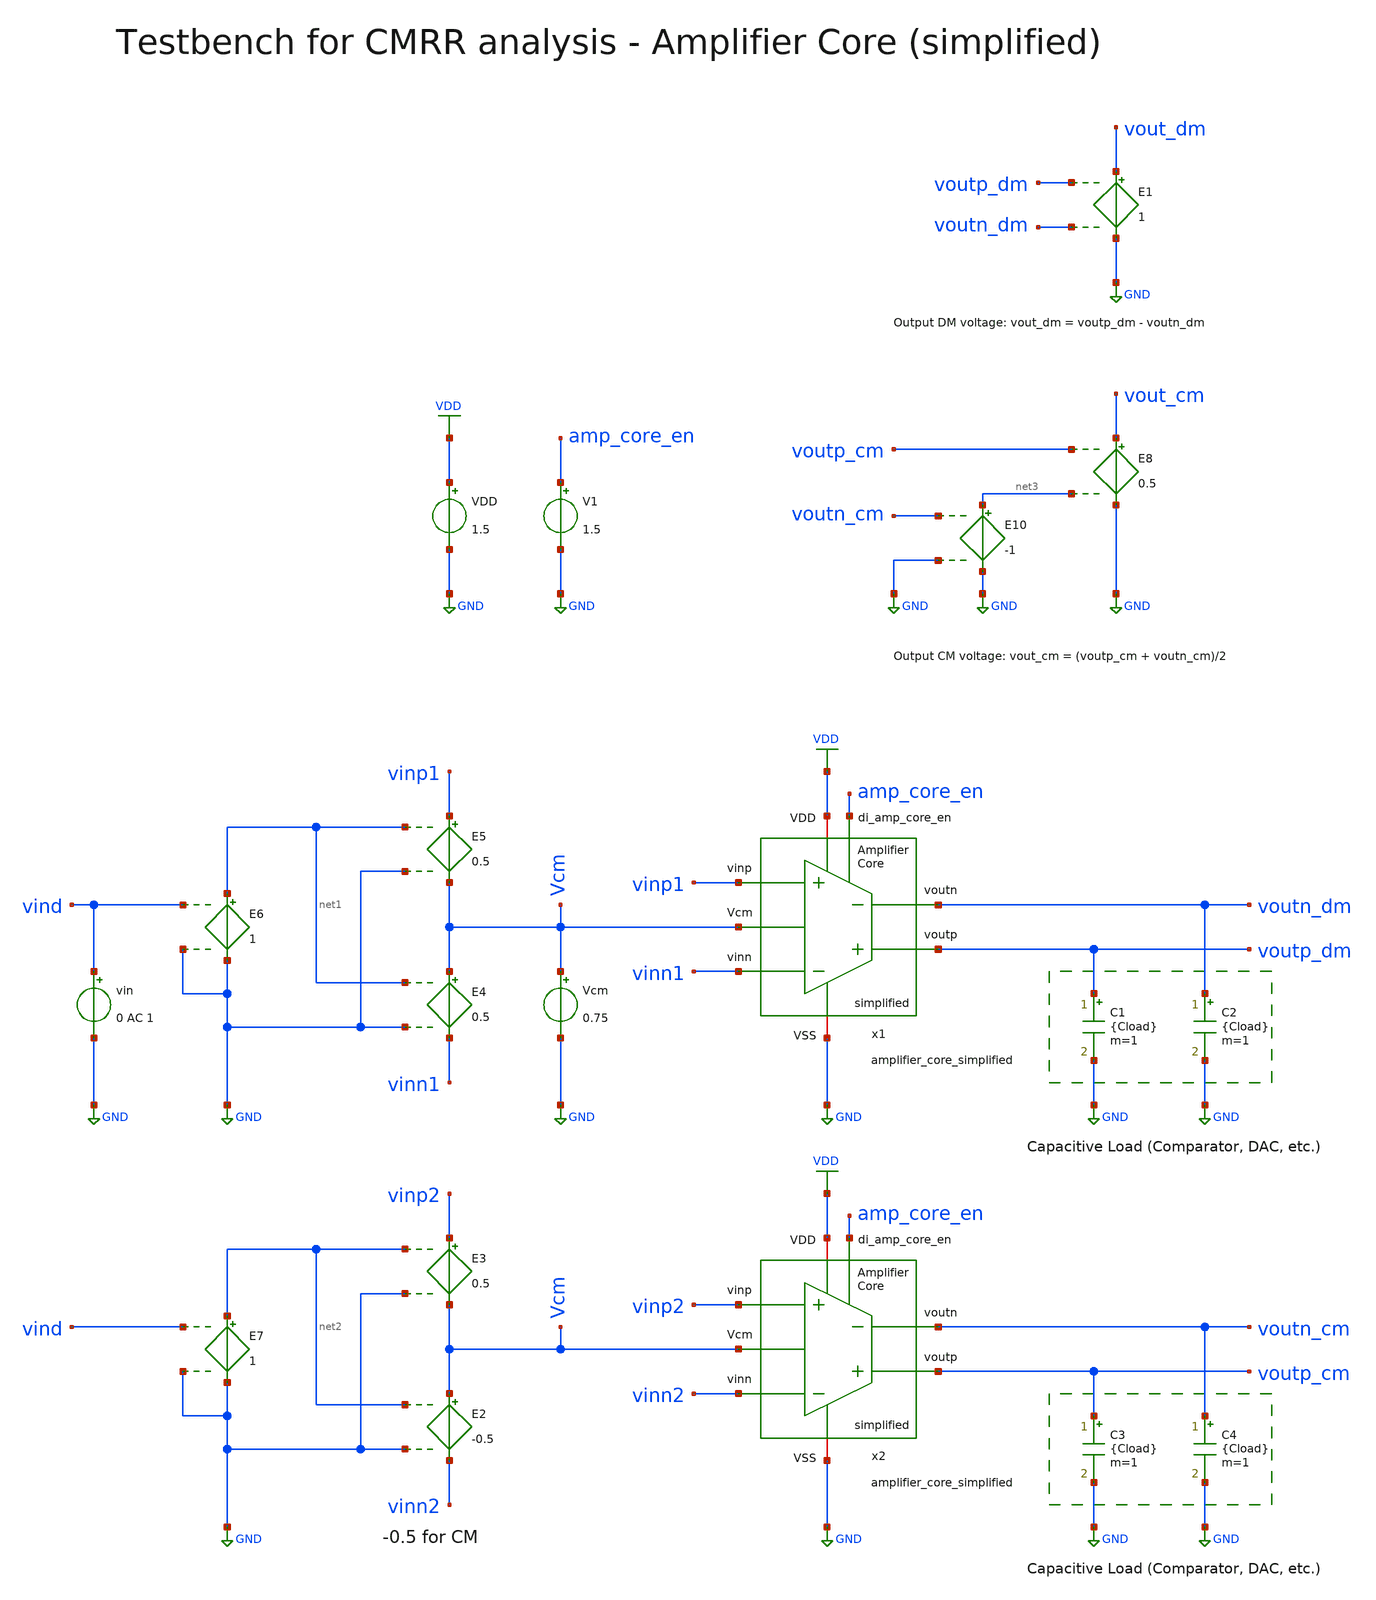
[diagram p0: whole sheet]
** sch_path: SG13G2_ATBS-ADC-main/xschem/bio_amplifier/amplifier_core/testbenches/amplifier_core_simplified_tb_CMRR.sch
**.subckt amplifier_core_simplified_tb_CMRR
VDD VDD GND 1.5
C1 voutp_dm GND {Cload} m=1
C2 voutn_dm GND {Cload} m=1
Vcm Vcm GND 0.75
E4 Vcm vinn1 net1 GND 0.5
E5 vinp1 Vcm net1 GND 0.5
E6 net1 GND vind GND 1
V1 amp_core_en GND 1.5
E1 vout_dm GND voutp_dm voutn_dm 1
vin vind GND 0 AC 1
x1 voutp_dm voutn_dm amp_core_en vinn1 vinp1 VDD GND Vcm amplifier_core_simplified
C3 voutp_cm GND {Cload} m=1
C4 voutn_cm GND {Cload} m=1
E2 Vcm vinn2 net2 GND -0.5
E3 vinp2 Vcm net2 GND 0.5
E7 net2 GND vind GND 1
x2 voutp_cm voutn_cm amp_core_en vinn2 vinp2 VDD GND Vcm amplifier_core_simplified
E8 vout_cm GND voutp_cm net3 0.5
E10 net3 GND voutn_cm GND -1
**** begin user architecture code


.param temp=27
* 228fF DAC + (1 - beta) * 3.3pF
.param Cload=3.49p
.options savecurrents method=gear reltol=1e-2 abstol=1e-15 gmin=1e-15 rshunt=1e15
.control

save v(vout_dm) v(vout_cm) v(vind)

set wr_vecnames
set wr_singlescale

* User Constants
let f_min = 10m
let f_max = 1G
let fdc = 1

* Operating Point Analysis
op
remzerovec
write amplifier_core_simplified_tb_CMRR.raw
set appendwrite

* AC Analysis
ac dec 101 $&const.f_min $&const.f_max
remzerovec
write amplifier_core_simplified_tb_CMRR.raw

* Plotting Differential Mode Gain
let Adm = v(vout_dm)/v(vind)
let Adm_dB = vdb(Adm)
let Adm_arg = 180/PI*cphase(Adm)
plot Adm_dB Adm_arg ylabel 'Magnitude, Phase'

* Plotting Common Mode Gain
let Acm = v(vout_cm)/v(vind)
let Acm_dB = vdb(Acm)
let Acm_arg = 180/PI*cphase(Acm)
plot Acm_dB Acm_arg ylabel 'Magnitude, Phase'

* Plotting Common Mode Rejection Ratio
* let CMRR = v(vout_dm)/v(vout_cm)
let CMRR = v(Adm)/v(Acm)
let CMRR_dB = vdb(CMRR)
* let CMRR_dB = Adm_dB - Acm_dB
let CMRR_arg = 180/PI*cphase(CMRR)
plot CMRR_dB CMRR_arg ylabel 'Magnitude, Phase'

* Measurements
meas ac CMRRdc_dB find CMRR_dB when frequency = fdc
print CMRRdc_dB

* Write Data
set wr_vecnames
set wr_singlescale
wrdata
+ /foss/designs/SG13G2_ATBS-ADC-main/python/plot_simulations/data/amplifier_core_simplified_tb_CMRR.txt v(Adm_dB) v(Adm_arg) v(Acm_dB) v(Acm_arg) v(CMRR_dB) v(CMRR_arg)

*quit
.endc



.lib cornerMOSlv.lib mos_tt
.lib cornerMOShv.lib mos_tt
.lib cornerRES.lib res_typ

**** end user architecture code
**.ends
.GLOBAL GND
.GLOBAL VDD
.end
